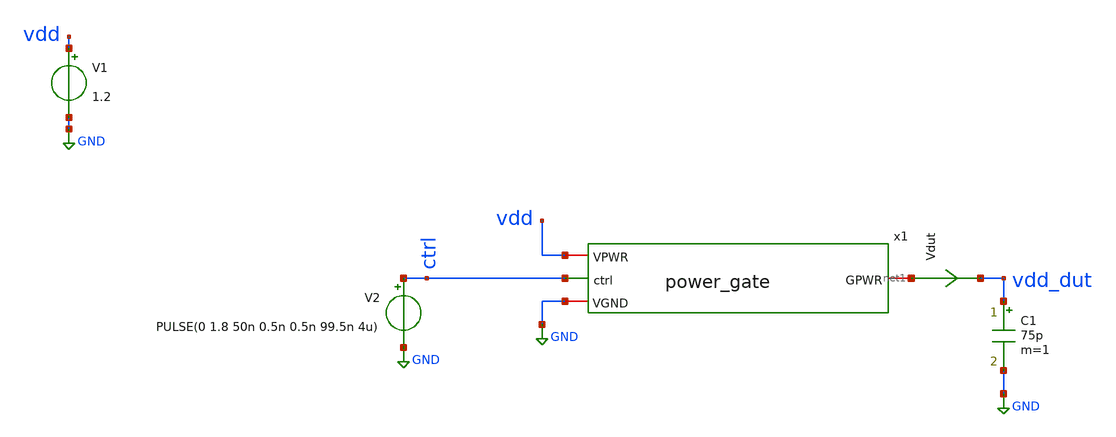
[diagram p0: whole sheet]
** sch_path: ihp-sg13cmos5l/libs.tech/xschem/tests/tb_power_gate.sch
**.subckt tb_power_gate
x1 vdd net1 ctrl GND power_gate
V1 vdd GND 1.2
.save i(v1)
V2 ctrl GND PULSE(0 1.8 50n 0.5n 0.5n 99.5n 4u)
C1 vdd_dut GND 75p m=1
Vdut net1 vdd_dut 0
.save i(vdut)
**** begin user architecture code

.lib cornerMOSlv.lib mos_tt
*.lib cornerCAP.lib cap_typ



.param mc_mm_switch=0
.control
save all
tran 50p 5u
plot vdd_dut
plot vdd_dut x1.ctrl_n ctrl xlimit 50n 60n
*quit 0
.endc
.end


**** end user architecture code
**.ends

* expanding   symbol:  hm_analog/power_gate.sym # of pins=4
** sym_path: ihp-sg13cmos5l/libs.tech/xschem/hm_analog/power_gate.sym
** sch_path: ihp-sg13cmos5l/libs.tech/xschem/hm_analog/power_gate.sch
.subckt power_gate VPWR GPWR ctrl VGND
*.ipin ctrl
*.iopin VPWR
*.iopin VGND
*.iopin GPWR
XM1 ctrl_n ctrl VGND VGND sg13_lv_nmos w=2.6u l=0.13u ng=1 m=1 mm_ok=1
XM2 ctrl_n ctrl VPWR VPWR sg13_lv_pmos w=4.44u l=0.13u ng=1 m=1 mm_ok=1
XM3 GPWR ctrl_n VPWR VPWR sg13_lv_pmos w=2175u l=0.13u ng=290 m=1 mm_ok=1
x1 VGND GPWR ctrl_n dischg
.ends


* expanding   symbol:
*+  /home/designer/shared/hm-openpdk-library/ihp-sg13cmos5l/libs.tech/xschem/hm_analog/dischg.sym # of pins=3
** sym_path: ihp-sg13cmos5l/libs.tech/xschem/hm_analog/dischg.sym
** sch_path: ihp-sg13cmos5l/libs.tech/xschem/hm_analog/dischg.sch
.subckt dischg VGND GPWR gate
*.iopin GPWR
*.iopin VGND
*.ipin gate
XM1 GPWR gate net2 VGND sg13_lv_nmos w=4u l=0.65u ng=1 m=1 mm_ok=1
XM2 net2 gate net3 VGND sg13_lv_nmos w=4u l=0.65u ng=1 m=1 mm_ok=1
XM3 net3 gate net4 VGND sg13_lv_nmos w=4u l=0.65u ng=1 m=1 mm_ok=1
XM4 net4 gate net1 VGND sg13_lv_nmos w=4u l=0.65u ng=1 m=1 mm_ok=1
XM5 net1 gate net7 VGND sg13_lv_nmos w=4u l=0.65u ng=1 m=1 mm_ok=1
XM6 net7 gate net6 VGND sg13_lv_nmos w=4u l=0.65u ng=1 m=1 mm_ok=1
XM7 net6 gate net5 VGND sg13_lv_nmos w=4u l=0.65u ng=1 m=1 mm_ok=1
XM8 net5 gate VGND VGND sg13_lv_nmos w=4u l=0.65u ng=1 m=1 mm_ok=1
XM9 GPWR gate net9 VGND sg13_lv_nmos w=4u l=0.65u ng=1 m=1 mm_ok=1
XM10 net9 gate net10 VGND sg13_lv_nmos w=4u l=0.65u ng=1 m=1 mm_ok=1
XM11 net10 gate net11 VGND sg13_lv_nmos w=4u l=0.65u ng=1 m=1 mm_ok=1
XM12 net11 gate net8 VGND sg13_lv_nmos w=4u l=0.65u ng=1 m=1 mm_ok=1
XM13 net8 gate net14 VGND sg13_lv_nmos w=4u l=0.65u ng=1 m=1 mm_ok=1
XM14 net14 gate net13 VGND sg13_lv_nmos w=4u l=0.65u ng=1 m=1 mm_ok=1
XM15 net13 gate net12 VGND sg13_lv_nmos w=4u l=0.65u ng=1 m=1 mm_ok=1
XM16 net12 gate VGND VGND sg13_lv_nmos w=4u l=0.65u ng=1 m=1 mm_ok=1
.ends

.GLOBAL GND
.end
